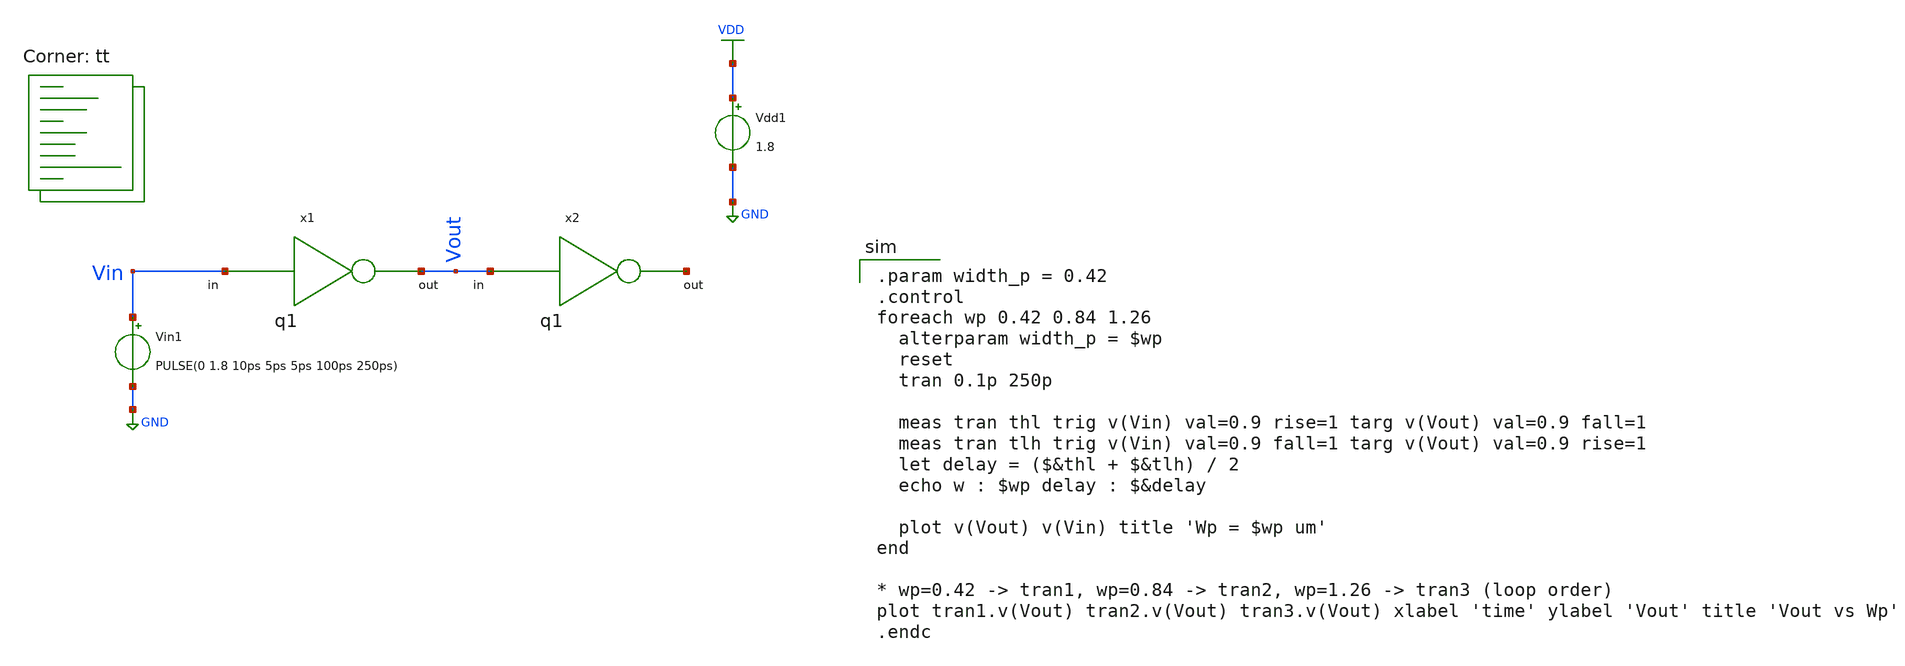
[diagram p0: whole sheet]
** sch_path: tutorial-3/source/q1a.sch
**.subckt q1a
x1 Vout Vin q1
x2 net1 Vout q1
Vin1 Vin GND PULSE(0 1.8 10ps 5ps 5ps 100ps 250ps)
Vdd1 VDD GND 1.8
**** begin user architecture code
.lib $::SKYWATER_MODELS/sky130.lib.spice tt

.param width_p = 0.42
.control
foreach wp 0.42 0.84 1.26
  alterparam width_p = $wp
  reset
  tran 0.1p 250p

  meas tran thl trig v(Vin) val=0.9 rise=1 targ v(Vout) val=0.9 fall=1
  meas tran tlh trig v(Vin) val=0.9 fall=1 targ v(Vout) val=0.9 rise=1
  let delay = ($&thl + $&tlh) / 2
  echo w : $wp delay : $&delay

  plot v(Vout) v(Vin) title 'Wp = $wp um'
end

* wp=0.42 -> tran1, wp=0.84 -> tran2, wp=1.26 -> tran3 (loop order)
plot tran1.v(Vout) tran2.v(Vout) tran3.v(Vout) xlabel 'time' ylabel 'Vout' title 'Vout vs Wp'
.endc

**** end user architecture code
**.ends

* expanding   symbol:  q1.sym # of pins=2
** sym_path: tutorial-3/source/q1.sym
** sch_path: tutorial-3/source/q1.sch
.subckt q1 out in
*.ipin in
*.opin out
XM1 out in VDD VDD sky130_fd_pr__pfet_01v8 L=0.15 W={width_p} nf=1 ad='int((nf+1)/2) * W/nf * 0.29' as='int((nf+2)/2) * W/nf * 0.29'
+ pd='2*int((nf+1)/2) * (W/nf + 0.29)' ps='2*int((nf+2)/2) * (W/nf + 0.29)' nrd='0.29 / W' nrs='0.29 / W'
+ sa=0 sb=0 sd=0 mult=1 m=1
XM2 out in GND GND sky130_fd_pr__nfet_01v8 L=0.15 W=0.42 nf=1 ad='int((nf+1)/2) * W/nf * 0.29' as='int((nf+2)/2) * W/nf * 0.29'
+ pd='2*int((nf+1)/2) * (W/nf + 0.29)' ps='2*int((nf+2)/2) * (W/nf + 0.29)' nrd='0.29 / W' nrs='0.29 / W'
+ sa=0 sb=0 sd=0 mult=1 m=1
.ends

.GLOBAL GND
.GLOBAL VDD
.end
